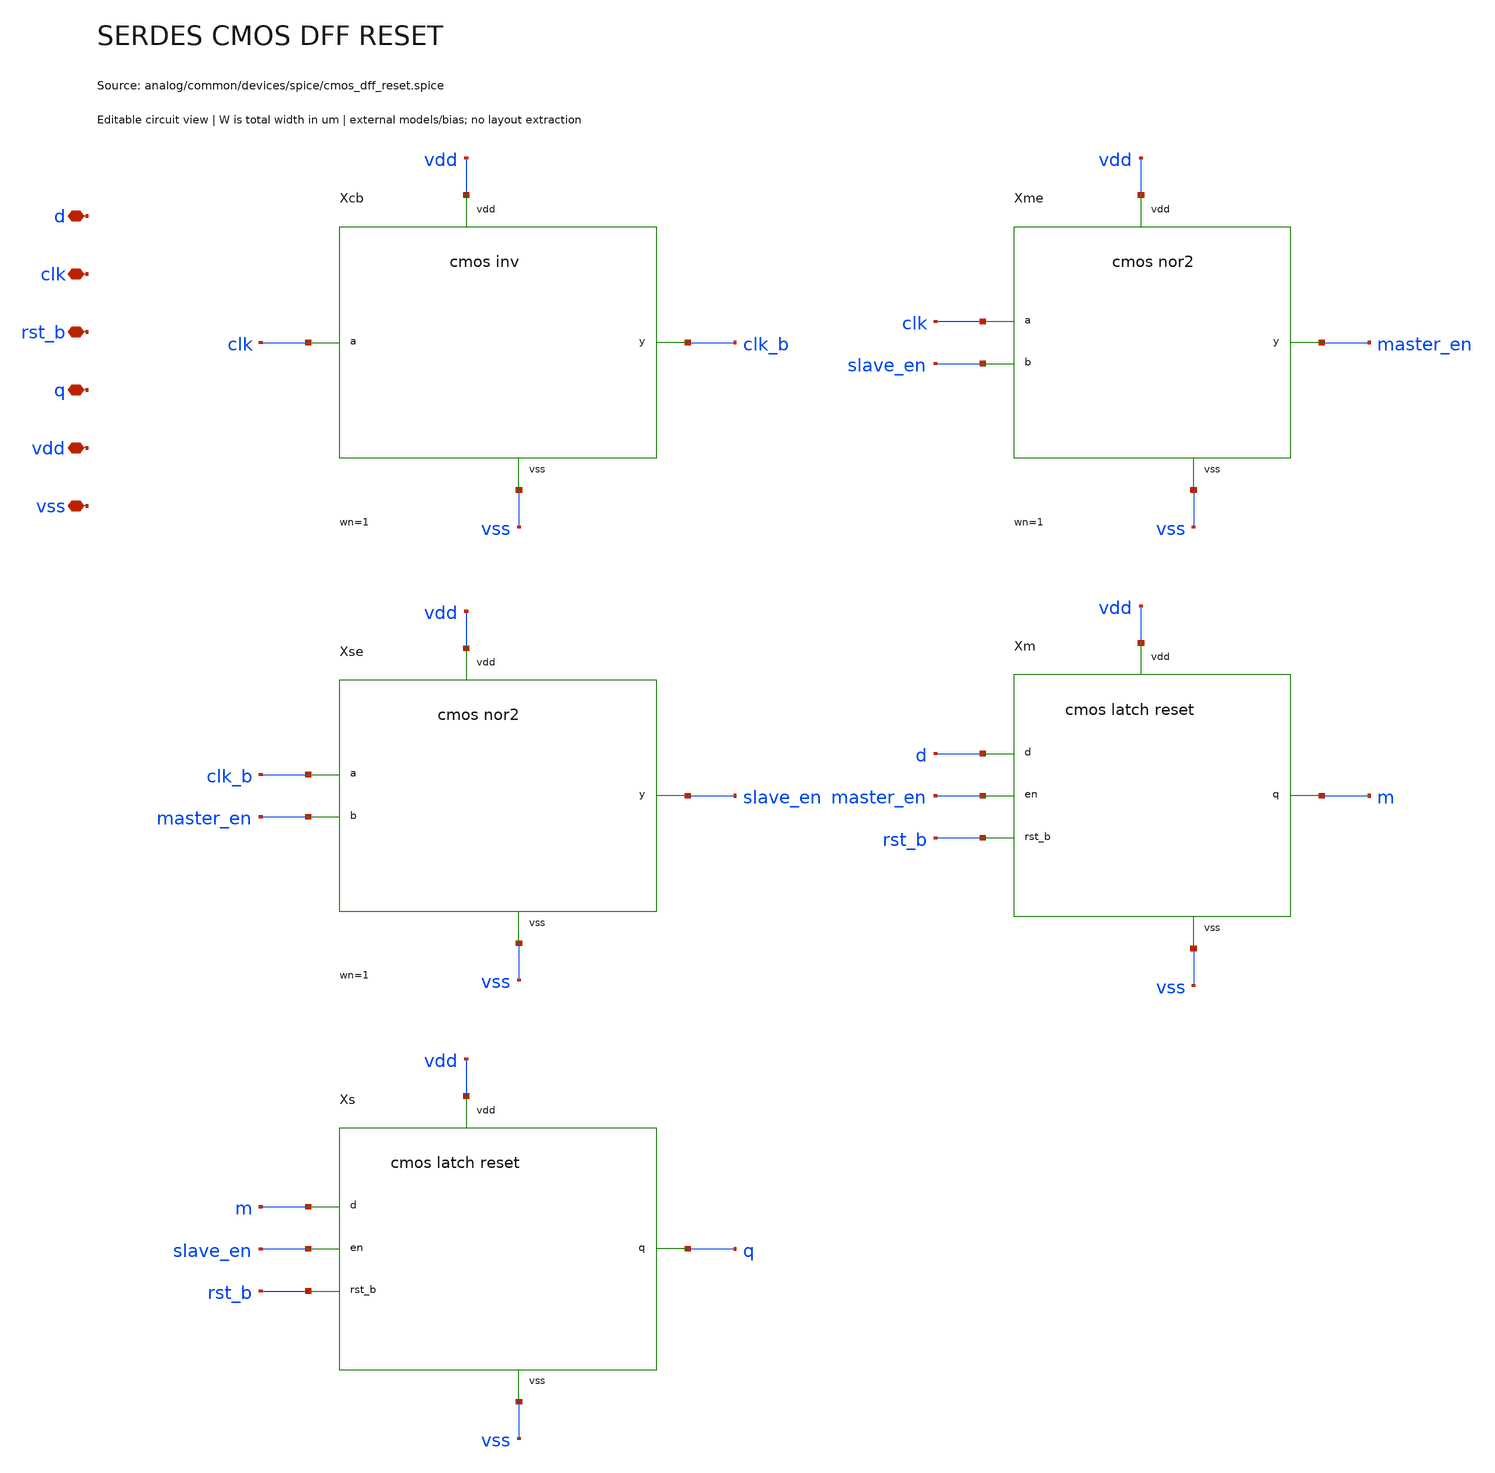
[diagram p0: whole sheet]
** sch_path: analog/common/devices/schematic/serdes_cmos_dff_reset.sch
**.subckt serdes_cmos_dff_reset d clk rst_b q vdd vss
*.iopin d
*.iopin clk
*.iopin rst_b
*.iopin q
*.iopin vdd
*.iopin vss
Xcb clk clk_b vdd vss serdes_cmos_inv wn=1 wp=2
Xme clk slave_en master_en vdd vss serdes_cmos_nor2 wn=1 wp=4
Xse clk_b master_en slave_en vdd vss serdes_cmos_nor2 wn=1 wp=4
Xm d master_en rst_b m vdd vss serdes_cmos_latch_reset
Xs m slave_en rst_b q vdd vss serdes_cmos_latch_reset
**.ends

* expanding   symbol:  serdes/serdes_cmos_inv.sym # of pins=4
** sym_path: analog/common/devices/schematic/serdes_cmos_inv.sym
** sch_path: analog/common/devices/schematic/serdes_cmos_inv.sch
.subckt serdes_cmos_inv a y vdd vss  wn=1 wp=2
*.iopin a
*.iopin y
*.iopin vdd
*.iopin vss
Xn y a vss vss serdes_nfet w={wn} l=0.15 nf=1
Xp y a vdd vdd serdes_pfet w={wp} l=0.15 nf=1
.ends


* expanding   symbol:  serdes/serdes_cmos_nor2.sym # of pins=5
** sym_path: analog/common/devices/schematic/serdes_cmos_nor2.sym
** sch_path: analog/common/devices/schematic/serdes_cmos_nor2.sch
.subckt serdes_cmos_nor2 a b y vdd vss  wn=1 wp=4
*.iopin a
*.iopin b
*.iopin y
*.iopin vdd
*.iopin vss
Xna y a vss vss serdes_nfet w={wn} l=0.15 nf=1
Xnb y b vss vss serdes_nfet w={wn} l=0.15 nf=1
Xpa y a mid vdd serdes_pfet w={wp} l=0.15 nf=1
Xpb mid b vdd vdd serdes_pfet w={wp} l=0.15 nf=1
.ends


* expanding   symbol:  serdes/serdes_cmos_latch_reset.sym # of pins=6
** sym_path: analog/common/devices/schematic/serdes_cmos_latch_reset.sym
** sch_path: analog/common/devices/schematic/serdes_cmos_latch_reset.sch
.subckt serdes_cmos_latch_reset d en rst_b q vdd vss
*.iopin d
*.iopin en
*.iopin rst_b
*.iopin q
*.iopin vdd
*.iopin vss
Xeb en en_b vdd vss serdes_cmos_inv wn=1 wp=2
Xpn en rst_b pass_b vdd vss serdes_cmos_nand2 wn=2 wp=2
Xpi pass_b pass vdd vss serdes_cmos_inv wn=1 wp=2
Xhn en_b rst_b hold_b vdd vss serdes_cmos_nand2 wn=2 wp=2
Xhi hold_b hold vdd vss serdes_cmos_inv wn=1 wp=2
Xr rst_b rst vdd vss serdes_cmos_inv wn=1 wp=2
Xpass d x pass pass_b vdd vss serdes_cmos_tgate wn=1 wp=2
Xhold q x hold hold_b vdd vss serdes_cmos_tgate wn=1 wp=2
Xreset x rst vss vss serdes_nfet w=4 l=0.15 nf=1
Xi x q_b vdd vss serdes_cmos_inv wn=1 wp=2
Xo q_b q vdd vss serdes_cmos_inv wn=1 wp=2
.ends


* expanding   symbol:  serdes/serdes_nfet.sym # of pins=4
** sym_path: analog/common/devices/schematic/serdes_nfet.sym
** sch_path: analog/common/devices/schematic/serdes_nfet.sch
.subckt serdes_nfet d g s b  w=1 l=0.15 nf=1
*.iopin d
*.iopin g
*.iopin s
*.iopin b
Xmos d g s b sky130_fd_pr__nfet_01v8 w={w} l={l} nf={nf} ad={floor((nf+1)/2)*(w/nf)*0.29} as={floor((nf+2)/2)*(w/nf)*0.29}
+ pd={2*floor((nf+1)/2)*(w/nf+0.29)} ps={2*floor((nf+2)/2)*(w/nf+0.29)}
.ends


* expanding   symbol:  serdes/serdes_pfet.sym # of pins=4
** sym_path: analog/common/devices/schematic/serdes_pfet.sym
** sch_path: analog/common/devices/schematic/serdes_pfet.sch
.subckt serdes_pfet d g s b  w=3 l=0.15 nf=1
*.iopin d
*.iopin g
*.iopin s
*.iopin b
Xmos d g s b sky130_fd_pr__pfet_01v8 w={w} l={l} nf={nf} ad={floor((nf+1)/2)*(w/nf)*0.29} as={floor((nf+2)/2)*(w/nf)*0.29}
+ pd={2*floor((nf+1)/2)*(w/nf+0.29)} ps={2*floor((nf+2)/2)*(w/nf+0.29)}
.ends


* expanding   symbol:  serdes/serdes_cmos_nand2.sym # of pins=5
** sym_path: analog/common/devices/schematic/serdes_cmos_nand2.sym
** sch_path: analog/common/devices/schematic/serdes_cmos_nand2.sch
.subckt serdes_cmos_nand2 a b y vdd vss  wn=2 wp=2
*.iopin a
*.iopin b
*.iopin y
*.iopin vdd
*.iopin vss
Xna y a mid vss serdes_nfet w={wn} l=0.15 nf=1
Xnb mid b vss vss serdes_nfet w={wn} l=0.15 nf=1
Xpa y a vdd vdd serdes_pfet w={wp} l=0.15 nf=1
Xpb y b vdd vdd serdes_pfet w={wp} l=0.15 nf=1
.ends


* expanding   symbol:  serdes/serdes_cmos_tgate.sym # of pins=6
** sym_path: analog/common/devices/schematic/serdes_cmos_tgate.sym
** sch_path: analog/common/devices/schematic/serdes_cmos_tgate.sch
.subckt serdes_cmos_tgate a b en en_b vdd vss  wn=1 wp=2
*.iopin a
*.iopin b
*.iopin en
*.iopin en_b
*.iopin vdd
*.iopin vss
Xn a en b vss serdes_nfet w={wn} l=0.15 nf=1
Xp a en_b b vdd serdes_pfet w={wp} l=0.15 nf=1
.ends

.end
